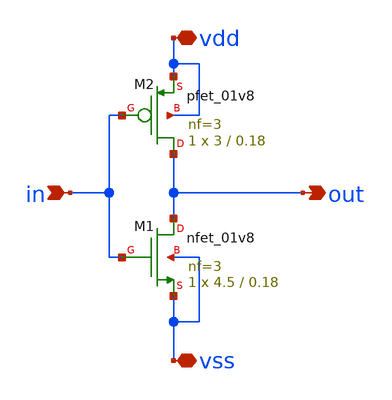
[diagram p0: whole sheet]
** sch_path: Lab1_inverter/xschem/inverter_1.sch
**.subckt inverter_1 in out vdd vss
*.ipin in
*.opin out
*.iopin vdd
*.iopin vss
XM1 out in vss vss sky130_fd_pr__nfet_01v8 L=0.18 W=4.5 nf=3 ad='int((3 + 1)/2) * 4.5 / 3 * 0.29' as='int((3 + 2)/2) * 4.5 / 3 * 0.29'
+ pd='2*int((3 + 1)/2) * (4.5 / 3 + 0.29)' ps='2*int((3 + 2)/2) * (4.5 / 3 + 0.29)' nrd='0.29 / 4.5 ' nrs='0.29 / 4.5 '
+ sa=0 sb=0 sd=0 mult=1 m=1
XM2 out in vdd vdd sky130_fd_pr__pfet_01v8 L=0.18 W=3 nf=3 ad='int((3 + 1)/2) * 3 / 3 * 0.29' as='int((3 + 2)/2) * 3 / 3 * 0.29'
+ pd='2*int((3 + 1)/2) * (3 / 3 + 0.29)' ps='2*int((3 + 2)/2) * (3 / 3 + 0.29)' nrd='0.29 / 3 ' nrs='0.29 / 3 '
+ sa=0 sb=0 sd=0 mult=1 m=1
**.ends
.end
